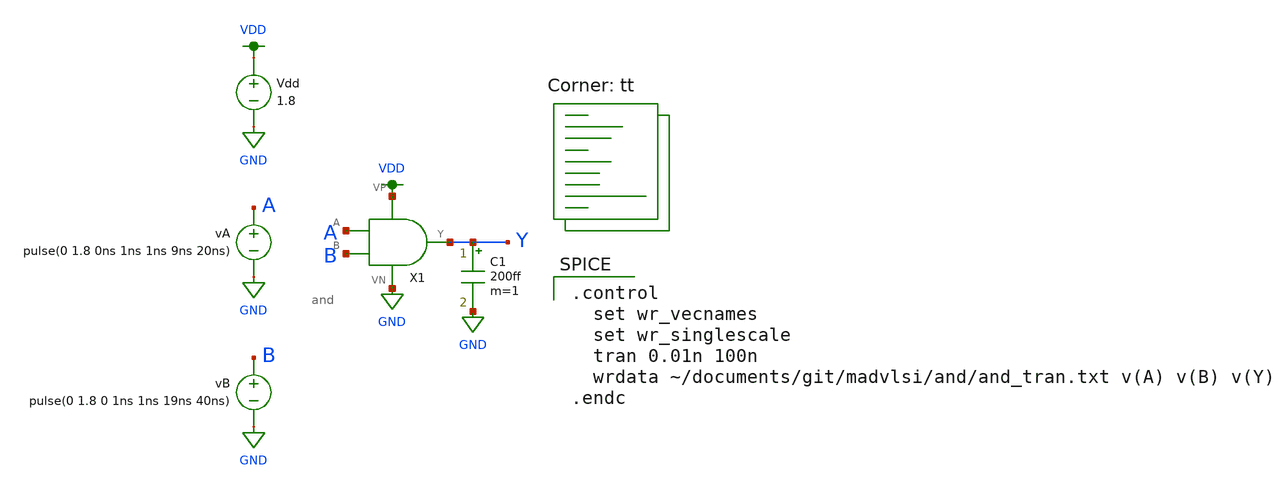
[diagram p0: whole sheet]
** sch_path: and/schematic/and_tran.sch
**.subckt and_tran
Vdd VDD GND 1.8
vA A GND pulse(0 1.8 0ns 1ns 1ns 9ns 20ns)
vB B GND pulse(0 1.8 0 1ns 1ns 19ns 40ns)
X1 A Y VDD GND B and
C1 Y GND 200ff m=1
**** begin user architecture code

.control
  set wr_vecnames
  set wr_singlescale
  tran 0.01n 100n
  wrdata ~/documents/git/madvlsi/and/and_tran.txt v(A) v(B) v(Y)
.endc

.lib $::SKYWATER_MODELS/sky130.lib.spice tt
**** end user architecture code
**.ends
.GLOBAL GND
.GLOBAL VDD
.end
